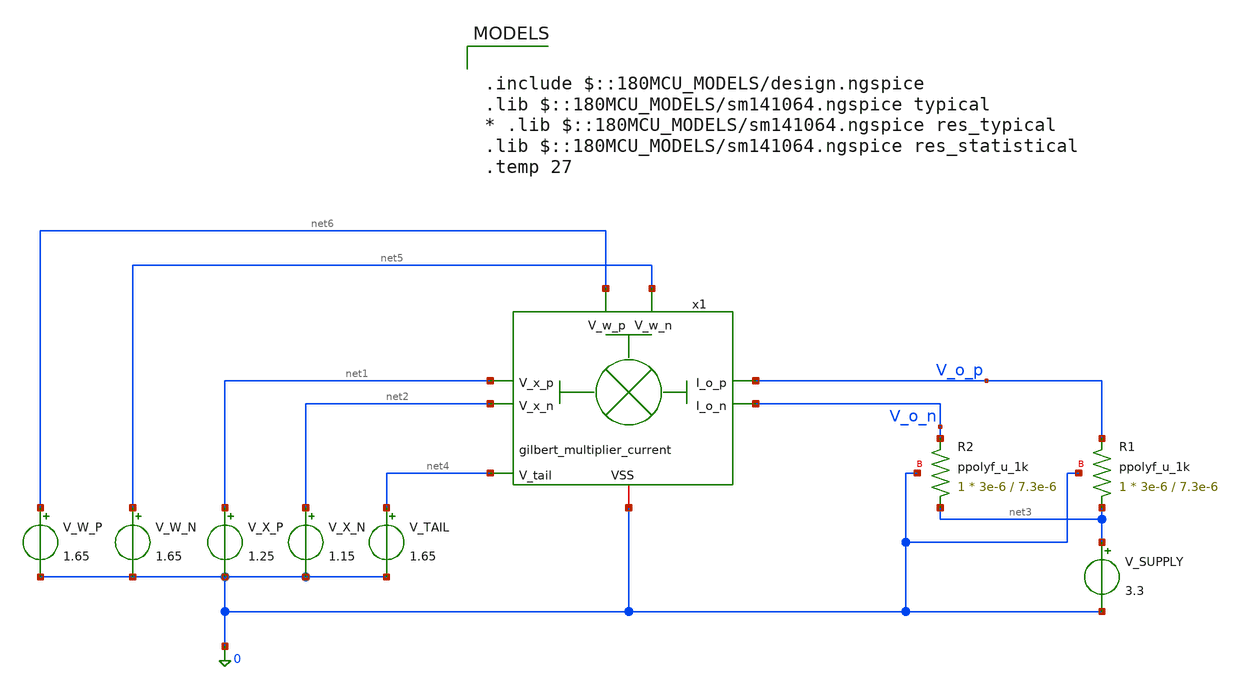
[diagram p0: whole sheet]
** sch_path: lvs/schematics/tb_gilbert_multiplier_current.sch
**.subckt tb_gilbert_multiplier_current
V_X_P net1 0 1.25
V_X_N net2 0 1.15
V_W_P net6 0 1.65
V_W_N net5 0 1.65
V_SUPPLY net3 0 3.3
XR1 net3 V_o_p 0 ppolyf_u_1k r_width=3e-6 r_length=7.3e-6 m=1
XR2 net3 V_o_n 0 ppolyf_u_1k r_width=3e-6 r_length=7.3e-6 m=1
V_TAIL net4 0 1.65
x1 V_o_p V_o_n net6 net5 net1 net2 net4 0 gilbert_multiplier_current
**** begin user architecture code


.control
  op
  echo "--- Gilbert cell x1: transistor op points ---"
  print @m.x1.xm1.m0[vgs] @m.x1.xm1.m0[vth] @m.x1.xm1.m0[vdsat] @m.x1.xm1.m0[id] @m.x1.xm1.m0[gm]
+ @m.x1.xm1.m0[gds]
  print @m.x1.xm2.m0[vgs] @m.x1.xm2.m0[vth] @m.x1.xm2.m0[vdsat] @m.x1.xm2.m0[id] @m.x1.xm2.m0[gm]
+ @m.x1.xm2.m0[gds]
  print @m.x1.xm3.m0[vgs] @m.x1.xm3.m0[vth] @m.x1.xm3.m0[vdsat] @m.x1.xm3.m0[id] @m.x1.xm3.m0[gm]
+ @m.x1.xm3.m0[gds]
  print @m.x1.xm4.m0[vgs] @m.x1.xm4.m0[vth] @m.x1.xm4.m0[vdsat] @m.x1.xm4.m0[id] @m.x1.xm4.m0[gm]
+ @m.x1.xm4.m0[gds]
  print @m.x1.xm5.m0[vgs] @m.x1.xm5.m0[vth] @m.x1.xm5.m0[vdsat] @m.x1.xm5.m0[id] @m.x1.xm5.m0[gm]
+ @m.x1.xm5.m0[gds]
  print @m.x1.xm6.m0[vgs] @m.x1.xm6.m0[vth] @m.x1.xm6.m0[vdsat] @m.x1.xm6.m0[id] @m.x1.xm6.m0[gm]
+ @m.x1.xm6.m0[gds]
  print @m.x1.xm7.m0[vgs] @m.x1.xm7.m0[vth] @m.x1.xm7.m0[vdsat] @m.x1.xm7.m0[id] @m.x1.xm7.m0[gm]
+ @m.x1.xm7.m0[gds]
  print @m.x1.xm8.m0[vgs] @m.x1.xm8.m0[vth] @m.x1.xm8.m0[vdsat] @m.x1.xm8.m0[id] @m.x1.xm8.m0[gm]
+ @m.x1.xm8.m0[gds]
  echo "--- Gilbert cell x1: tail resistor ---"
  print @r.x1.xr1.rt1[resistance] @r.x1.xr1.rt2[resistance]
  * === Single sweep: baseline transfer curve ===
  alter V_X_P = 1.25
  alter V_X_N = 1.15
  dc V_W_P 1.15 2.15 0.01
  let V_diff_single = v(V_o_p) - v(V_o_n)
  plot V_diff_single title "Gilbert Multiplier: Single Weight Sweep"
  wrdata /foss/designs/analog-perceptron-gf180mcu/plots/gilbert_single_sweep.txt V_diff_single

  setplot const
  * === Family of curves, one clean sweep per V_X_P step ===
  let n = 0
  dowhile n <= 4
    let vxp = 1.05 + n * 0.05
    alter V_X_P = vxp
    dc V_W_P 1.15 2.15 0.01
    let V_diff_fam = v(V_o_p) - v(V_o_n)
    wrdata /foss/designs/analog-perceptron-gf180mcu/plots/gilbert_family_sweep.txt V_diff_fam
    set appendwrite
    let n = n + 1
  end
  unset appendwrite

  alter V_X_P = 1.25
  alter V_X_N = 1.15
  alter V_W_P = 1.65
  * === OP-SWEEP DIAGNOSTIC: all 8 devices' headroom across full weight range ===
  alter V_X_P = 1.25
  alter V_X_N = 1.15
  save all @m.x1.xm1.m0[vgs] @m.x1.xm1.m0[vth] @m.x1.xm1.m0[vdsat] @m.x1.xm1.m0[id] @m.x1.xm1.m0[gm] @m.x1.xm1.m0[gds] @m.x1.xm2.m0[vgs] @m.x1.xm2.m0[vth] @m.x1.xm2.m0[vdsat] @m.x1.xm2.m0[id] @m.x1.xm2.m0[gm] @m.x1.xm2.m0[gds] @m.x1.xm3.m0[vgs] @m.x1.xm3.m0[vth] @m.x1.xm3.m0[vdsat] @m.x1.xm3.m0[id] @m.x1.xm3.m0[gm] @m.x1.xm3.m0[gds] @m.x1.xm4.m0[vgs] @m.x1.xm4.m0[vth] @m.x1.xm4.m0[vdsat] @m.x1.xm4.m0[id] @m.x1.xm4.m0[gm] @m.x1.xm4.m0[gds] @m.x1.xm5.m0[vgs] @m.x1.xm5.m0[vth] @m.x1.xm5.m0[vdsat] @m.x1.xm5.m0[id] @m.x1.xm5.m0[gm] @m.x1.xm5.m0[gds] @m.x1.xm6.m0[vgs] @m.x1.xm6.m0[vth] @m.x1.xm6.m0[vdsat] @m.x1.xm6.m0[id] @m.x1.xm6.m0[gm] @m.x1.xm6.m0[gds] @m.x1.xm7.m0[vgs] @m.x1.xm7.m0[vth] @m.x1.xm7.m0[vdsat] @m.x1.xm7.m0[id] @m.x1.xm7.m0[gm] @m.x1.xm7.m0[gds] @m.x1.xm8.m0[vgs] @m.x1.xm8.m0[vth] @m.x1.xm8.m0[vdsat] @m.x1.xm8.m0[id] @m.x1.xm8.m0[gm] @m.x1.xm8.m0[gds]
  dc V_W_P 1.15 2.15 0.01
  wrdata /foss/designs/analog-perceptron-gf180mcu/plots/opsweep_gilbert.txt v(V_o_p) v(V_o_n) @m.x1.xm1.m0[vgs] @m.x1.xm1.m0[vth] @m.x1.xm1.m0[vdsat] @m.x1.xm1.m0[id] @m.x1.xm1.m0[gm] @m.x1.xm1.m0[gds] @m.x1.xm2.m0[vgs] @m.x1.xm2.m0[vth] @m.x1.xm2.m0[vdsat] @m.x1.xm2.m0[id] @m.x1.xm2.m0[gm] @m.x1.xm2.m0[gds] @m.x1.xm3.m0[vgs] @m.x1.xm3.m0[vth] @m.x1.xm3.m0[vdsat] @m.x1.xm3.m0[id] @m.x1.xm3.m0[gm] @m.x1.xm3.m0[gds] @m.x1.xm4.m0[vgs] @m.x1.xm4.m0[vth] @m.x1.xm4.m0[vdsat] @m.x1.xm4.m0[id] @m.x1.xm4.m0[gm] @m.x1.xm4.m0[gds] @m.x1.xm5.m0[vgs] @m.x1.xm5.m0[vth] @m.x1.xm5.m0[vdsat] @m.x1.xm5.m0[id] @m.x1.xm5.m0[gm] @m.x1.xm5.m0[gds] @m.x1.xm6.m0[vgs] @m.x1.xm6.m0[vth] @m.x1.xm6.m0[vdsat] @m.x1.xm6.m0[id] @m.x1.xm6.m0[gm] @m.x1.xm6.m0[gds] @m.x1.xm7.m0[vgs] @m.x1.xm7.m0[vth] @m.x1.xm7.m0[vdsat] @m.x1.xm7.m0[id] @m.x1.xm7.m0[gm] @m.x1.xm7.m0[gds] @m.x1.xm8.m0[vgs] @m.x1.xm8.m0[vth] @m.x1.xm8.m0[vdsat] @m.x1.xm8.m0[id] @m.x1.xm8.m0[gm] @m.x1.xm8.m0[gds]
  alter V_X_P = 1.25
  alter V_X_N = 1.15
  alter V_W_P = 1.65
.endc



.include $::180MCU_MODELS/design.ngspice
.lib $::180MCU_MODELS/sm141064.ngspice typical
* .lib $::180MCU_MODELS/sm141064.ngspice res_typical
.lib $::180MCU_MODELS/sm141064.ngspice res_statistical
.temp 27

**** end user architecture code
**.ends

* expanding   symbol:  analog-perceptron-gf180mcu/lvs/schematics/gilbert_multiplier_current.sym # of pins=8
** sym_path: lvs/schematics/gilbert_multiplier_current.sym
** sch_path: lvs/schematics/gilbert_multiplier_current.sch
.subckt gilbert_multiplier_current I_o_p I_o_n V_w_p V_w_n V_x_p V_x_n V_tail VSS
*.ipin V_x_p
*.ipin V_x_n
*.ipin V_tail
*.iopin VSS
*.ipin V_w_p
*.ipin V_w_n
*.opin I_o_n
*.opin I_o_p
XM1 net1 V_x_p net3 VSS nfet_03v3 L=0.5u W=10u nf=1 ad='int((nf+1)/2) * W/nf * 0.18u' as='int((nf+2)/2)
+ * W/nf * 0.18u' pd='2*int((nf+1)/2) * (W/nf + 0.18u)' ps='2*int((nf+2)/2) * (W/nf + 0.18u)' nrd='0.18u
+ / W' nrs='0.18u / W' sa=0 sb=0 sd=0 m=1
XM2 net2 V_x_n net4 VSS nfet_03v3 L=0.5u W=10u nf=1 ad='int((nf+1)/2) * W/nf * 0.18u' as='int((nf+2)/2)
+ * W/nf * 0.18u' pd='2*int((nf+1)/2) * (W/nf + 0.18u)' ps='2*int((nf+2)/2) * (W/nf + 0.18u)' nrd='0.18u
+ / W' nrs='0.18u / W' sa=0 sb=0 sd=0 m=1
XM3 I_o_n V_w_p net1 VSS nfet_03v3 L=0.5u W=20u nf=1 ad='int((nf+1)/2) * W/nf * 0.18u' as='int((nf+2)/2)
+ * W/nf * 0.18u' pd='2*int((nf+1)/2) * (W/nf + 0.18u)' ps='2*int((nf+2)/2) * (W/nf + 0.18u)' nrd='0.18u
+ / W' nrs='0.18u / W' sa=0 sb=0 sd=0 m=1
XM4 I_o_p V_w_n net1 VSS nfet_03v3 L=0.5u W=20u nf=1 ad='int((nf+1)/2) * W/nf * 0.18u' as='int((nf+2)/2)
+ * W/nf * 0.18u' pd='2*int((nf+1)/2) * (W/nf + 0.18u)' ps='2*int((nf+2)/2) * (W/nf + 0.18u)' nrd='0.18u
+ / W' nrs='0.18u / W' sa=0 sb=0 sd=0 m=1
XM5 I_o_n V_w_n net2 VSS nfet_03v3 L=0.5u W=20u nf=1 ad='int((nf+1)/2) * W/nf * 0.18u' as='int((nf+2)/2)
+ * W/nf * 0.18u' pd='2*int((nf+1)/2) * (W/nf + 0.18u)' ps='2*int((nf+2)/2) * (W/nf + 0.18u)' nrd='0.18u
+ / W' nrs='0.18u / W' sa=0 sb=0 sd=0 m=1
XM6 I_o_p V_w_p net2 VSS nfet_03v3 L=0.5u W=20u nf=1 ad='int((nf+1)/2) * W/nf * 0.18u' as='int((nf+2)/2)
+ * W/nf * 0.18u' pd='2*int((nf+1)/2) * (W/nf + 0.18u)' ps='2*int((nf+2)/2) * (W/nf + 0.18u)' nrd='0.18u
+ / W' nrs='0.18u / W' sa=0 sb=0 sd=0 m=1
XM7 net3 V_tail VSS VSS nfet_03v3 L=1u W=8u nf=1 ad='int((nf+1)/2) * W/nf * 0.18u' as='int((nf+2)/2)
+ * W/nf * 0.18u' pd='2*int((nf+1)/2) * (W/nf + 0.18u)' ps='2*int((nf+2)/2) * (W/nf + 0.18u)' nrd='0.18u
+ / W' nrs='0.18u / W' sa=0 sb=0 sd=0 m=1
XM8 net4 V_tail VSS VSS nfet_03v3 L=1u W=8u nf=1 ad='int((nf+1)/2) * W/nf * 0.18u' as='int((nf+2)/2)
+ * W/nf * 0.18u' pd='2*int((nf+1)/2) * (W/nf + 0.18u)' ps='2*int((nf+2)/2) * (W/nf + 0.18u)' nrd='0.18u
+ / W' nrs='0.18u / W' sa=0 sb=0 sd=0 m=1
XR1 net3 net4 VSS ppolyf_u_1k r_width=3e-6 r_length=46.2e-6 m=1
XM9 I_o_n VSS VSS VSS nfet_03v3 L=0.5u W=5u nf=1 ad='int((nf+1)/2) * W/nf * 0.18u' as='int((nf+2)/2)
+ * W/nf * 0.18u' pd='2*int((nf+1)/2) * (W/nf + 0.18u)' ps='2*int((nf+2)/2) * (W/nf + 0.18u)' nrd='0.18u
+ / W' nrs='0.18u / W' sa=0 sb=0 sd=0 m=1
XM10 I_o_p VSS VSS VSS nfet_03v3 L=0.5u W=5u nf=1 ad='int((nf+1)/2) * W/nf * 0.18u' as='int((nf+2)/2)
+ * W/nf * 0.18u' pd='2*int((nf+1)/2) * (W/nf + 0.18u)' ps='2*int((nf+2)/2) * (W/nf + 0.18u)' nrd='0.18u
+ / W' nrs='0.18u / W' sa=0 sb=0 sd=0 m=1
XM11 net1 VSS VSS VSS nfet_03v3 L=0.5u W=10u nf=1 ad='int((nf+1)/2) * W/nf * 0.18u' as='int((nf+2)/2)
+ * W/nf * 0.18u' pd='2*int((nf+1)/2) * (W/nf + 0.18u)' ps='2*int((nf+2)/2) * (W/nf + 0.18u)' nrd='0.18u
+ / W' nrs='0.18u / W' sa=0 sb=0 sd=0 m=1
XM12 net2 VSS VSS VSS nfet_03v3 L=0.5u W=10u nf=1 ad='int((nf+1)/2) * W/nf * 0.18u' as='int((nf+2)/2)
+ * W/nf * 0.18u' pd='2*int((nf+1)/2) * (W/nf + 0.18u)' ps='2*int((nf+2)/2) * (W/nf + 0.18u)' nrd='0.18u
+ / W' nrs='0.18u / W' sa=0 sb=0 sd=0 m=1
XM13 net3 VSS VSS VSS nfet_03v3 L=1u W=8u nf=1 ad='int((nf+1)/2) * W/nf * 0.18u' as='int((nf+2)/2) *
+ W/nf * 0.18u' pd='2*int((nf+1)/2) * (W/nf + 0.18u)' ps='2*int((nf+2)/2) * (W/nf + 0.18u)' nrd='0.18u
+ / W' nrs='0.18u / W' sa=0 sb=0 sd=0 m=1
XM15 I_o_p VSS VSS VSS nfet_03v3 L=0.5u W=5u nf=1 ad='int((nf+1)/2) * W/nf * 0.18u' as='int((nf+2)/2)
+ * W/nf * 0.18u' pd='2*int((nf+1)/2) * (W/nf + 0.18u)' ps='2*int((nf+2)/2) * (W/nf + 0.18u)' nrd='0.18u
+ / W' nrs='0.18u / W' sa=0 sb=0 sd=0 m=1
XM16 I_o_n VSS VSS VSS nfet_03v3 L=0.5u W=5u nf=1 ad='int((nf+1)/2) * W/nf * 0.18u' as='int((nf+2)/2)
+ * W/nf * 0.18u' pd='2*int((nf+1)/2) * (W/nf + 0.18u)' ps='2*int((nf+2)/2) * (W/nf + 0.18u)' nrd='0.18u
+ / W' nrs='0.18u / W' sa=0 sb=0 sd=0 m=1
.ends

.end
